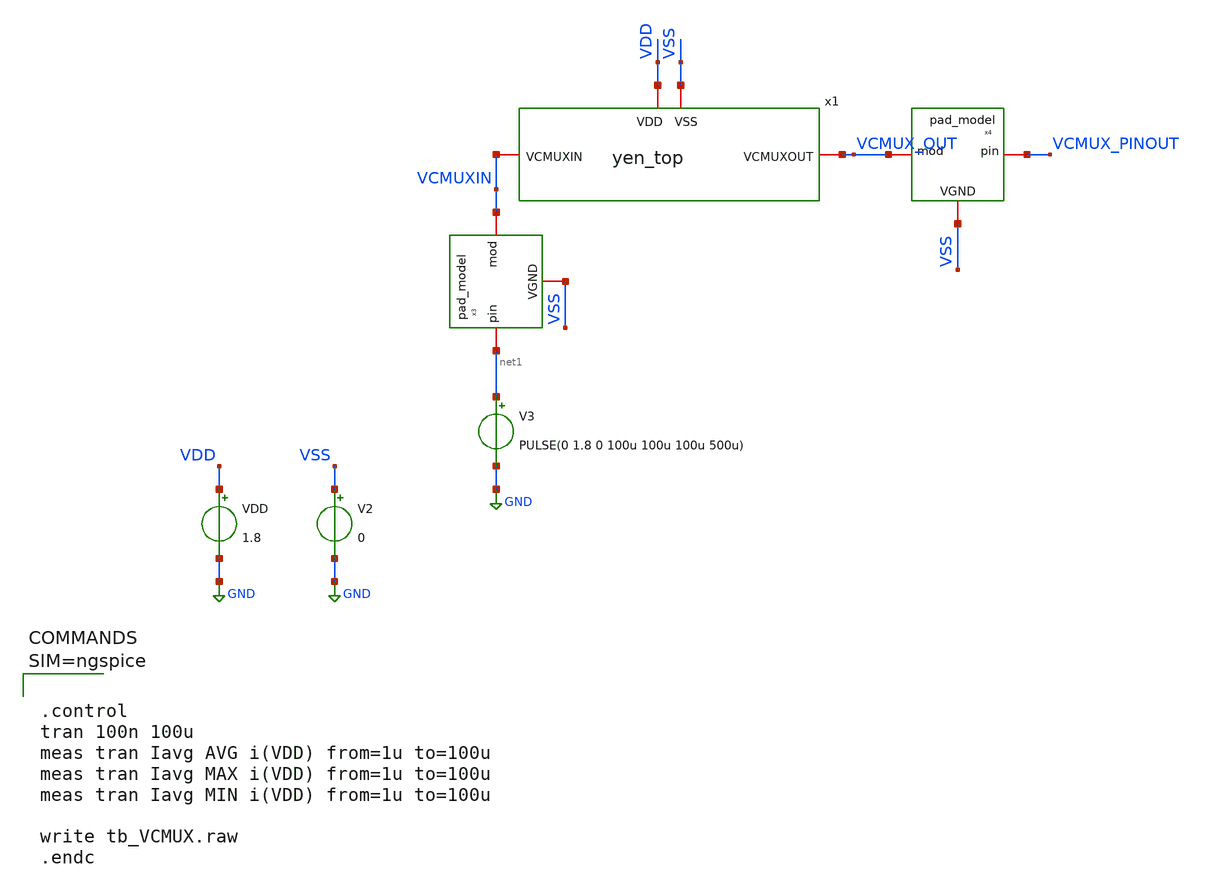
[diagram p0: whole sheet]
** sch_path: xschem/tb_VCMUX.sch
**.subckt tb_VCMUX
V2 VSS GND 0
x3 VSS net1 VCMUXIN pad_model
x4 VSS VCMUX_PINOUT VCMUX_OUT pad_model
VDD VDD GND 1.8
V3 net1 GND PULSE(0 1.8 0 100u 100u 100u 500u)
x1 VDD VSS VCMUXIN VCMUX_OUT yen_top
**** begin user architecture code

** opencircuitdesign pdks install
.lib $::SKYWATER_MODELS/sky130.lib.spice tt





.control
tran 100n 100u
meas tran Iavg AVG i(VDD) from=1u to=100u
meas tran Iavg MAX i(VDD) from=1u to=100u
meas tran Iavg MIN i(VDD) from=1u to=100u

write tb_VCMUX.raw
.endc



**** end user architecture code
**.ends
.GLOBAL GND
.end
